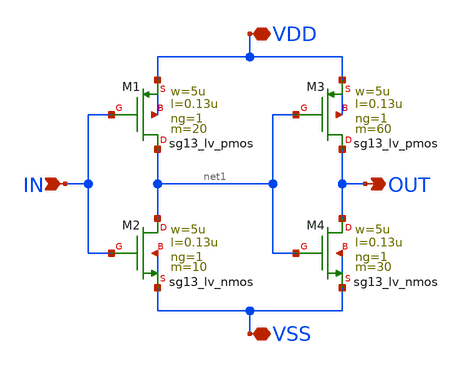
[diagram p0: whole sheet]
** sch_path: SSDOR_1V_v1/components/trans_gate_low/tg_low_noninverbuff.sch
**.subckt tg_low_noninverbuff VSS VDD IN OUT
*.iopin VSS
*.iopin VDD
*.ipin IN
*.opin OUT
XM1 net1 IN VDD VDD sg13_lv_pmos w=5u l=0.13u ng=1 m=20 mm_ok=1
XM2 net1 IN VSS VSS sg13_lv_nmos w=5u l=0.13u ng=1 m=10 mm_ok=1
XM3 OUT net1 VDD VDD sg13_lv_pmos w=5u l=0.13u ng=1 m=60 mm_ok=1
XM4 OUT net1 VSS VSS sg13_lv_nmos w=5u l=0.13u ng=1 m=30 mm_ok=1
**.ends
.end
